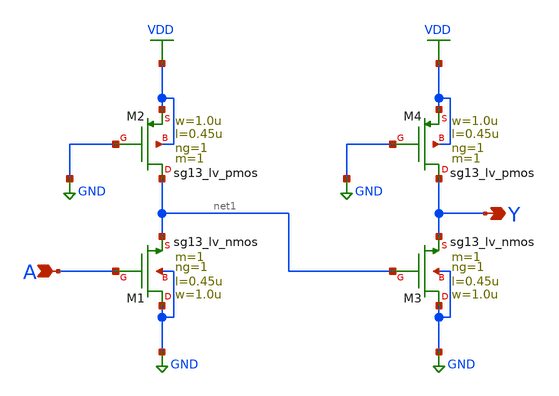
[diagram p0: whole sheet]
** sch_path: zip_meiners/ic_design/design_clkgen/inverter/better_inv.sch
**.subckt better_inv A Y
*.ipin A
*.opin Y
XM1 GND A net1 GND sg13_lv_nmos w=1.0u l=0.45u ng=1 m=1 mm_ok=1
XM2 net1 GND VDD VDD sg13_lv_pmos w=1.0u l=0.45u ng=1 m=1 mm_ok=1
XM3 GND net1 Y GND sg13_lv_nmos w=1.0u l=0.45u ng=1 m=1 mm_ok=1
XM4 Y GND VDD VDD sg13_lv_pmos w=1.0u l=0.45u ng=1 m=1 mm_ok=1
**.ends
.GLOBAL GND
.GLOBAL VDD
.end
